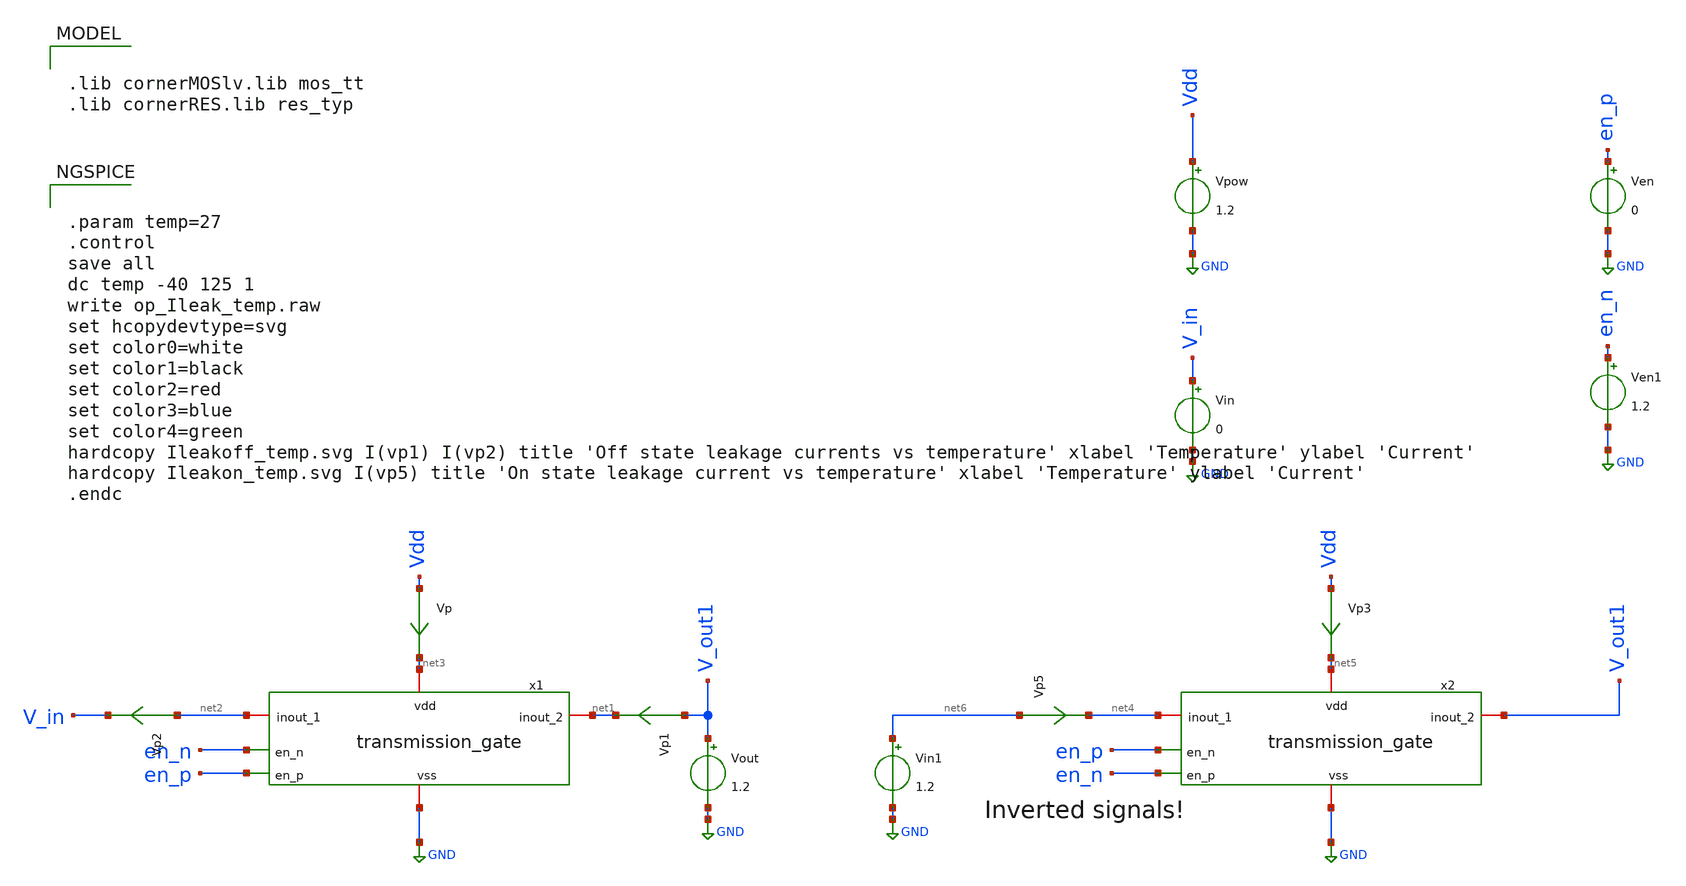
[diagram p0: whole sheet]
** sch_path: CHIPCHILE_CANELOS24_WorkshopTO/design_data/xschem/tgate/transmission_gate_tb_Ileak_temp.sch
* Copyright 2023 IHP PDK Authors
**.subckt transmission_gate_tb_Ileak_temp
Vpow Vdd GND 1.2
Vp Vdd net3 0
.save i(vp)
Vin V_in GND 0
Ven en_p GND 0
Ven1 en_n GND 1.2
x1 net3 en_n net2 net1 en_p GND transmission_gate
Vout V_out1 GND 1.2
Vp1 V_out1 net1 0
.save i(vp1)
Vp2 net2 V_in 0
.save i(vp2)
Vp3 Vdd net5 0
.save i(vp3)
x2 net5 en_p net4 V_out1 en_n GND transmission_gate
Vp5 net6 net4 0
.save i(vp5)
Vin1 net6 GND 1.2
**** begin user architecture code

.lib cornerMOSlv.lib mos_tt
.lib cornerRES.lib res_typ



.param temp=27
.control
save all
dc temp -40 125 1
write op_Ileak_temp.raw
set hcopydevtype=svg
set color0=white
set color1=black
set color2=red
set color3=blue
set color4=green
hardcopy Ileakoff_temp.svg I(vp1) I(vp2) title 'Off state leakage currents vs temperature' xlabel 'Temperature'
+ ylabel 'Current'
hardcopy Ileakon_temp.svg I(vp5) title 'On state leakage current vs temperature' xlabel 'Temperature'
+ ylabel 'Current'
.endc


**** end user architecture code
**.ends

* expanding   symbol:  transmission_gate.sym # of pins=6
** sym_path: CHIPCHILE_CANELOS24_WorkshopTO/design_data/xschem/multiplexer/transmission_gate.sym
** sch_path: CHIPCHILE_CANELOS24_WorkshopTO/design_data/xschem/multiplexer/transmission_gate.sch
.subckt transmission_gate vdd en_n inout_1 inout_2 en_p vss
*.iopin inout_1
*.iopin inout_2
*.ipin en_p
*.iopin vdd
*.iopin vss
*.ipin en_n
XM1 inout_1 en_p inout_2 net1 sg13_lv_nmos w=200.0u l=0.130u ng=20 m=1 mm_ok=1
XM2 inout_1 en_n inout_2 net2 sg13_lv_pmos w=200.0u l=0.130u ng=20 m=1 mm_ok=1
XR1 vdd net2 ntap1 R=262.8 w=0.78e-6 l=0.78e-6
XR2 vss net1 ptap1 R=262.8 w=0.78e-6 l=0.78e-6
.ends

.GLOBAL GND
.end
